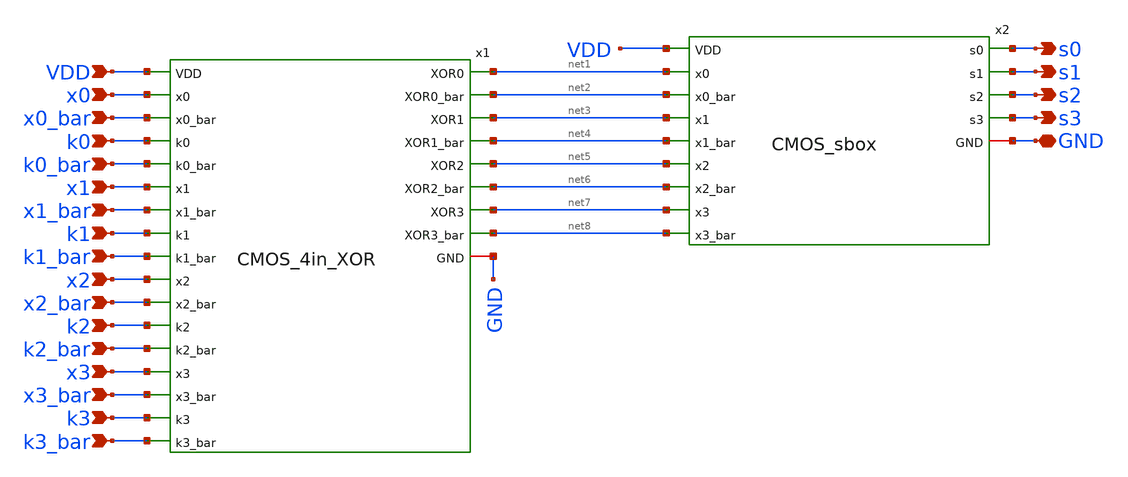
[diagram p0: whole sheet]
** sch_path: skywater_stuff/CMOS_PRESENT80_R1_flat.sch
**.subckt CMOS_PRESENT80_R1_flat GND k0 k0_bar x0 x0_bar x1_bar x1 k1_bar k1 k2 k2_bar x2 x2_bar
*+ x3_bar x3 k3_bar k3 s3 s2 s1 s0 VDD
*.iopin GND
*.ipin k0
*.ipin k0_bar
*.ipin x0
*.ipin x0_bar
*.ipin x1_bar
*.ipin x1
*.ipin k1_bar
*.ipin k1
*.ipin k2
*.ipin k2_bar
*.ipin x2
*.ipin x2_bar
*.ipin x3_bar
*.ipin x3
*.ipin k3_bar
*.ipin k3
*.opin s3
*.opin s2
*.opin s1
*.opin s0
*.ipin VDD
x2 s0 VDD net1 net2 net3 net4 net5 net6 net7 net8 s1 s2 s3 GND CMOS_sbox
x1 VDD net1 x0 net2 x0_bar k0 k0_bar net3 x1 net4 x1_bar k1 k1_bar net5 x2 x2_bar net6 k2 k2_bar
+ net7 x3 GND net8 x3_bar k3 k3_bar CMOS_4in_XOR
**.ends
.end
